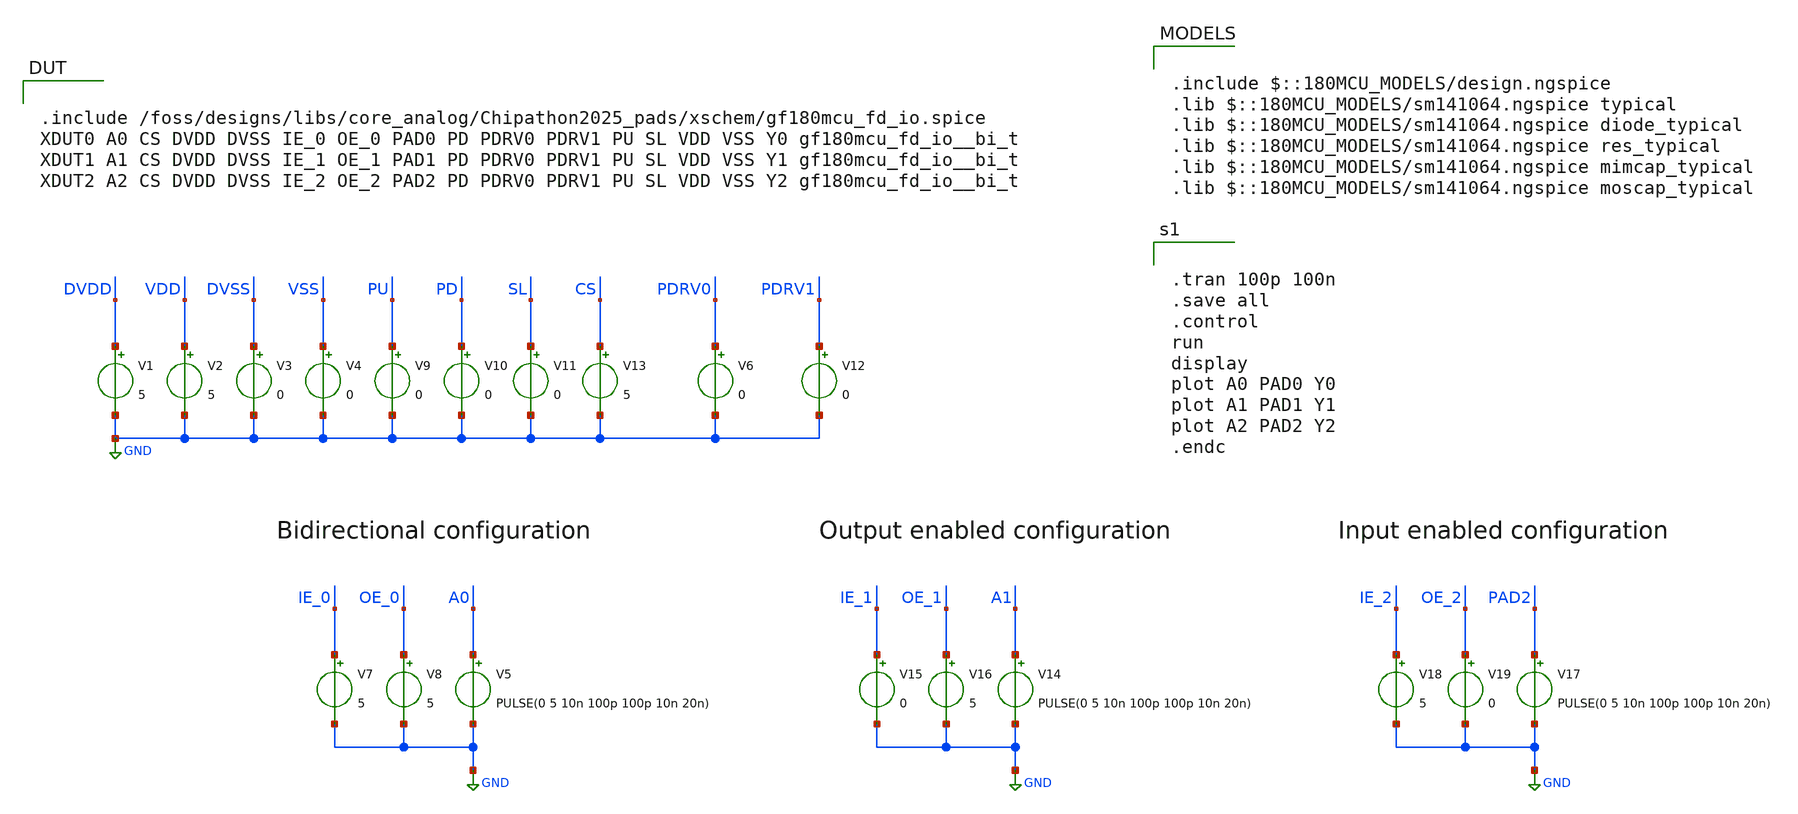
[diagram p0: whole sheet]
** sch_path: designs/libs/core_analog/Chipathon2025_pads/xschem/bi_t_tran_tb.sch
**.subckt bi_t_tran_tb
V1 DVDD GND 5
V2 VDD GND 5
V3 DVSS GND 0
V4 VSS GND 0
V5 A0 GND PULSE(0 5 10n 100p 100p 10n 20n)
V7 IE_0 GND 5
V8 OE_0 GND 5
V9 PU GND 0
V10 PD GND 0
V11 SL GND 0
V13 CS GND 5
V6 PDRV0 GND 0
V12 PDRV1 GND 0
V14 A1 GND PULSE(0 5 10n 100p 100p 10n 20n)
V15 IE_1 GND 0
V16 OE_1 GND 5
V17 PAD2 GND PULSE(0 5 10n 100p 100p 10n 20n)
V18 IE_2 GND 5
V19 OE_2 GND 0
**** begin user architecture code


.tran 100p 100n
.save all
.control
run
display
plot A0 PAD0 Y0
plot A1 PAD1 Y1
plot A2 PAD2 Y2
.endc



.include $::180MCU_MODELS/design.ngspice
.lib $::180MCU_MODELS/sm141064.ngspice typical
.lib $::180MCU_MODELS/sm141064.ngspice diode_typical
.lib $::180MCU_MODELS/sm141064.ngspice res_typical
.lib $::180MCU_MODELS/sm141064.ngspice mimcap_typical
.lib $::180MCU_MODELS/sm141064.ngspice moscap_typical


.include /foss/designs/libs/core_analog/Chipathon2025_pads/xschem/gf180mcu_fd_io.spice
XDUT0 A0 CS DVDD DVSS IE_0 OE_0 PAD0 PD PDRV0 PDRV1 PU SL VDD VSS Y0 gf180mcu_fd_io__bi_t
XDUT1 A1 CS DVDD DVSS IE_1 OE_1 PAD1 PD PDRV0 PDRV1 PU SL VDD VSS Y1 gf180mcu_fd_io__bi_t
XDUT2 A2 CS DVDD DVSS IE_2 OE_2 PAD2 PD PDRV0 PDRV1 PU SL VDD VSS Y2 gf180mcu_fd_io__bi_t

**** end user architecture code
**.ends
.GLOBAL GND
.end
